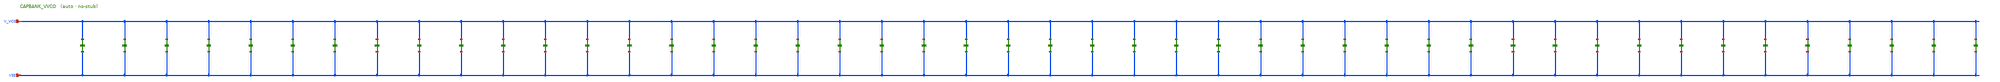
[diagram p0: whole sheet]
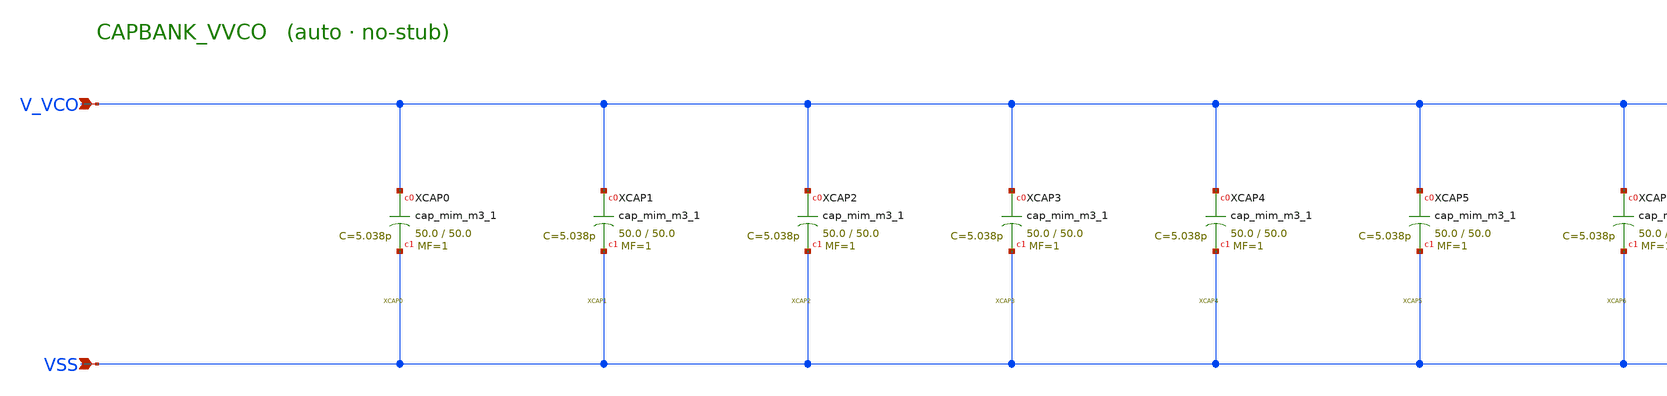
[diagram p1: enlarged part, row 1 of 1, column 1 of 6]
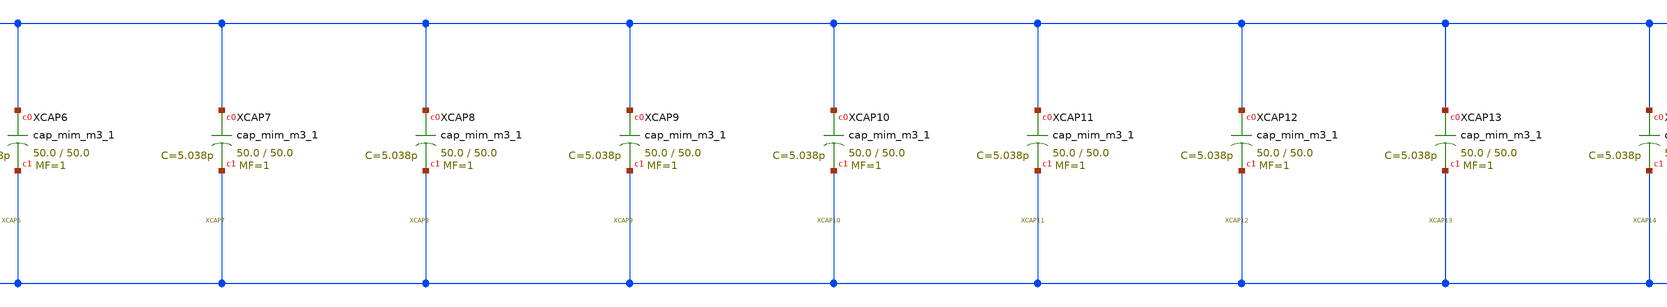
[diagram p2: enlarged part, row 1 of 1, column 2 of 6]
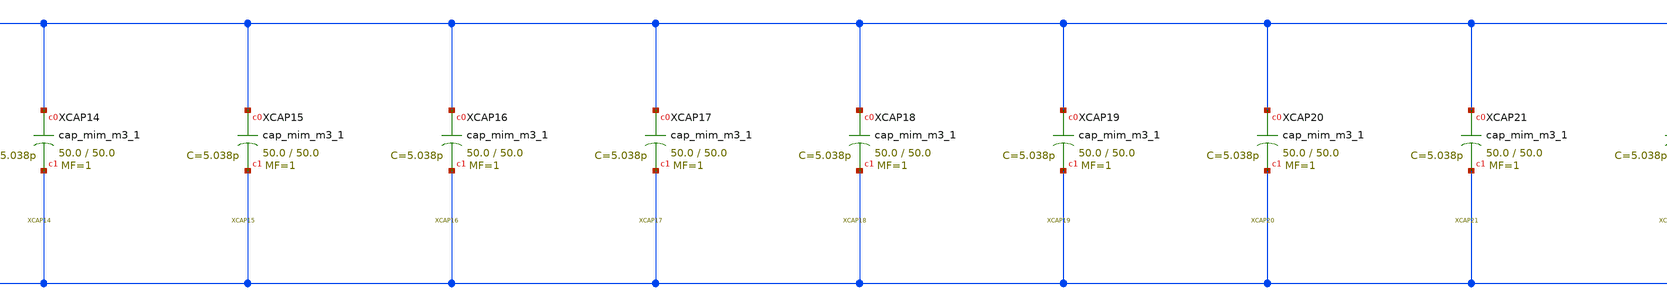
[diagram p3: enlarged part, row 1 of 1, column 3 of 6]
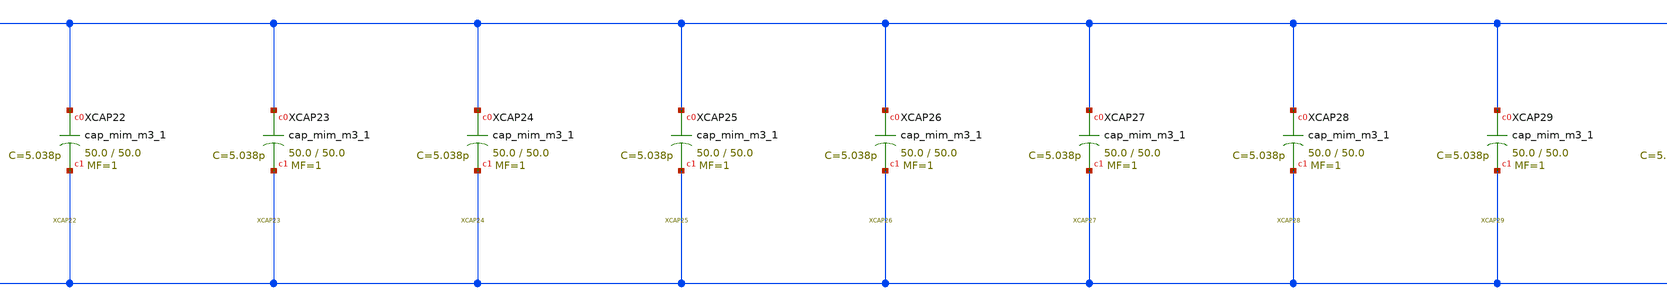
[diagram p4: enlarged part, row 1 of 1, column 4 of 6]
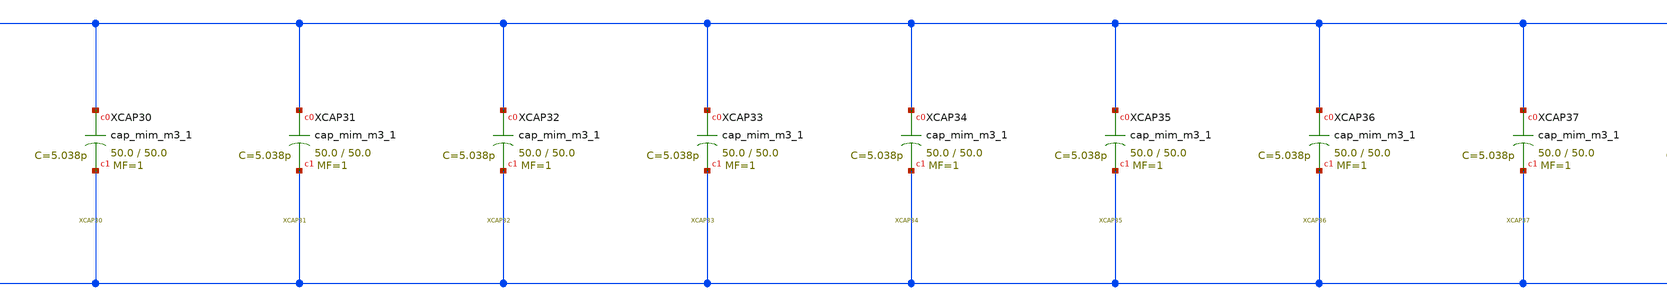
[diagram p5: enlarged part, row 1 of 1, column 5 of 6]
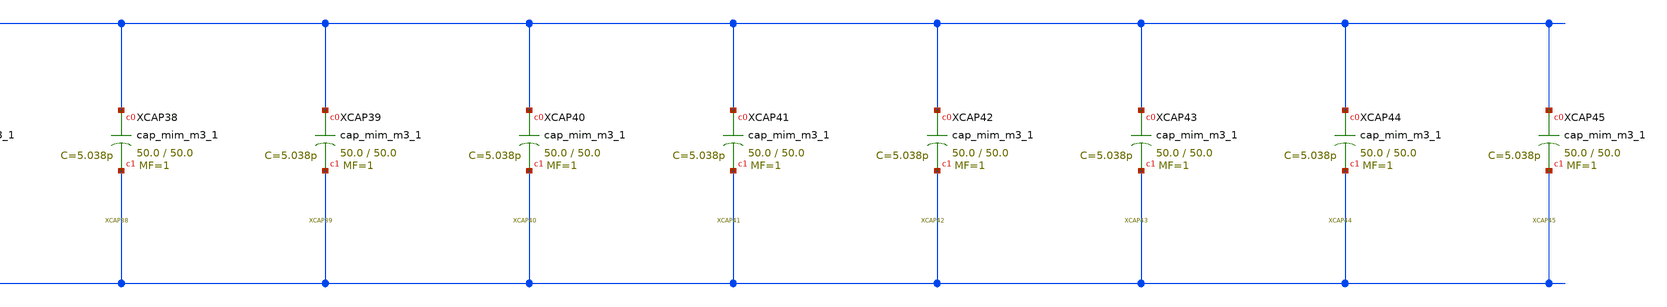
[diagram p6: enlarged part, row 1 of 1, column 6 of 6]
** sch_path: schematics/CAPBANK_VVCO.sch
**.subckt CAPBANK_VVCO VSS V_VCO
*.ipin VSS
*.ipin V_VCO
XXCAP0 V_VCO VSS sky130_fd_pr__cap_mim_m3_1 W=50.0 L=50.0 MF=1 m=1
XXCAP1 V_VCO VSS sky130_fd_pr__cap_mim_m3_1 W=50.0 L=50.0 MF=1 m=1
XXCAP2 V_VCO VSS sky130_fd_pr__cap_mim_m3_1 W=50.0 L=50.0 MF=1 m=1
XXCAP3 V_VCO VSS sky130_fd_pr__cap_mim_m3_1 W=50.0 L=50.0 MF=1 m=1
XXCAP4 V_VCO VSS sky130_fd_pr__cap_mim_m3_1 W=50.0 L=50.0 MF=1 m=1
XXCAP5 V_VCO VSS sky130_fd_pr__cap_mim_m3_1 W=50.0 L=50.0 MF=1 m=1
XXCAP6 V_VCO VSS sky130_fd_pr__cap_mim_m3_1 W=50.0 L=50.0 MF=1 m=1
XXCAP7 V_VCO VSS sky130_fd_pr__cap_mim_m3_1 W=50.0 L=50.0 MF=1 m=1
XXCAP8 V_VCO VSS sky130_fd_pr__cap_mim_m3_1 W=50.0 L=50.0 MF=1 m=1
XXCAP9 V_VCO VSS sky130_fd_pr__cap_mim_m3_1 W=50.0 L=50.0 MF=1 m=1
XXCAP10 V_VCO VSS sky130_fd_pr__cap_mim_m3_1 W=50.0 L=50.0 MF=1 m=1
XXCAP11 V_VCO VSS sky130_fd_pr__cap_mim_m3_1 W=50.0 L=50.0 MF=1 m=1
XXCAP12 V_VCO VSS sky130_fd_pr__cap_mim_m3_1 W=50.0 L=50.0 MF=1 m=1
XXCAP13 V_VCO VSS sky130_fd_pr__cap_mim_m3_1 W=50.0 L=50.0 MF=1 m=1
XXCAP14 V_VCO VSS sky130_fd_pr__cap_mim_m3_1 W=50.0 L=50.0 MF=1 m=1
XXCAP15 V_VCO VSS sky130_fd_pr__cap_mim_m3_1 W=50.0 L=50.0 MF=1 m=1
XXCAP16 V_VCO VSS sky130_fd_pr__cap_mim_m3_1 W=50.0 L=50.0 MF=1 m=1
XXCAP17 V_VCO VSS sky130_fd_pr__cap_mim_m3_1 W=50.0 L=50.0 MF=1 m=1
XXCAP18 V_VCO VSS sky130_fd_pr__cap_mim_m3_1 W=50.0 L=50.0 MF=1 m=1
XXCAP19 V_VCO VSS sky130_fd_pr__cap_mim_m3_1 W=50.0 L=50.0 MF=1 m=1
XXCAP20 V_VCO VSS sky130_fd_pr__cap_mim_m3_1 W=50.0 L=50.0 MF=1 m=1
XXCAP21 V_VCO VSS sky130_fd_pr__cap_mim_m3_1 W=50.0 L=50.0 MF=1 m=1
XXCAP22 V_VCO VSS sky130_fd_pr__cap_mim_m3_1 W=50.0 L=50.0 MF=1 m=1
XXCAP23 V_VCO VSS sky130_fd_pr__cap_mim_m3_1 W=50.0 L=50.0 MF=1 m=1
XXCAP24 V_VCO VSS sky130_fd_pr__cap_mim_m3_1 W=50.0 L=50.0 MF=1 m=1
XXCAP25 V_VCO VSS sky130_fd_pr__cap_mim_m3_1 W=50.0 L=50.0 MF=1 m=1
XXCAP26 V_VCO VSS sky130_fd_pr__cap_mim_m3_1 W=50.0 L=50.0 MF=1 m=1
XXCAP27 V_VCO VSS sky130_fd_pr__cap_mim_m3_1 W=50.0 L=50.0 MF=1 m=1
XXCAP28 V_VCO VSS sky130_fd_pr__cap_mim_m3_1 W=50.0 L=50.0 MF=1 m=1
XXCAP29 V_VCO VSS sky130_fd_pr__cap_mim_m3_1 W=50.0 L=50.0 MF=1 m=1
XXCAP30 V_VCO VSS sky130_fd_pr__cap_mim_m3_1 W=50.0 L=50.0 MF=1 m=1
XXCAP31 V_VCO VSS sky130_fd_pr__cap_mim_m3_1 W=50.0 L=50.0 MF=1 m=1
XXCAP32 V_VCO VSS sky130_fd_pr__cap_mim_m3_1 W=50.0 L=50.0 MF=1 m=1
XXCAP33 V_VCO VSS sky130_fd_pr__cap_mim_m3_1 W=50.0 L=50.0 MF=1 m=1
XXCAP34 V_VCO VSS sky130_fd_pr__cap_mim_m3_1 W=50.0 L=50.0 MF=1 m=1
XXCAP35 V_VCO VSS sky130_fd_pr__cap_mim_m3_1 W=50.0 L=50.0 MF=1 m=1
XXCAP36 V_VCO VSS sky130_fd_pr__cap_mim_m3_1 W=50.0 L=50.0 MF=1 m=1
XXCAP37 V_VCO VSS sky130_fd_pr__cap_mim_m3_1 W=50.0 L=50.0 MF=1 m=1
XXCAP38 V_VCO VSS sky130_fd_pr__cap_mim_m3_1 W=50.0 L=50.0 MF=1 m=1
XXCAP39 V_VCO VSS sky130_fd_pr__cap_mim_m3_1 W=50.0 L=50.0 MF=1 m=1
XXCAP40 V_VCO VSS sky130_fd_pr__cap_mim_m3_1 W=50.0 L=50.0 MF=1 m=1
XXCAP41 V_VCO VSS sky130_fd_pr__cap_mim_m3_1 W=50.0 L=50.0 MF=1 m=1
XXCAP42 V_VCO VSS sky130_fd_pr__cap_mim_m3_1 W=50.0 L=50.0 MF=1 m=1
XXCAP43 V_VCO VSS sky130_fd_pr__cap_mim_m3_1 W=50.0 L=50.0 MF=1 m=1
XXCAP44 V_VCO VSS sky130_fd_pr__cap_mim_m3_1 W=50.0 L=50.0 MF=1 m=1
XXCAP45 V_VCO VSS sky130_fd_pr__cap_mim_m3_1 W=50.0 L=50.0 MF=1 m=1
**.ends
.end
